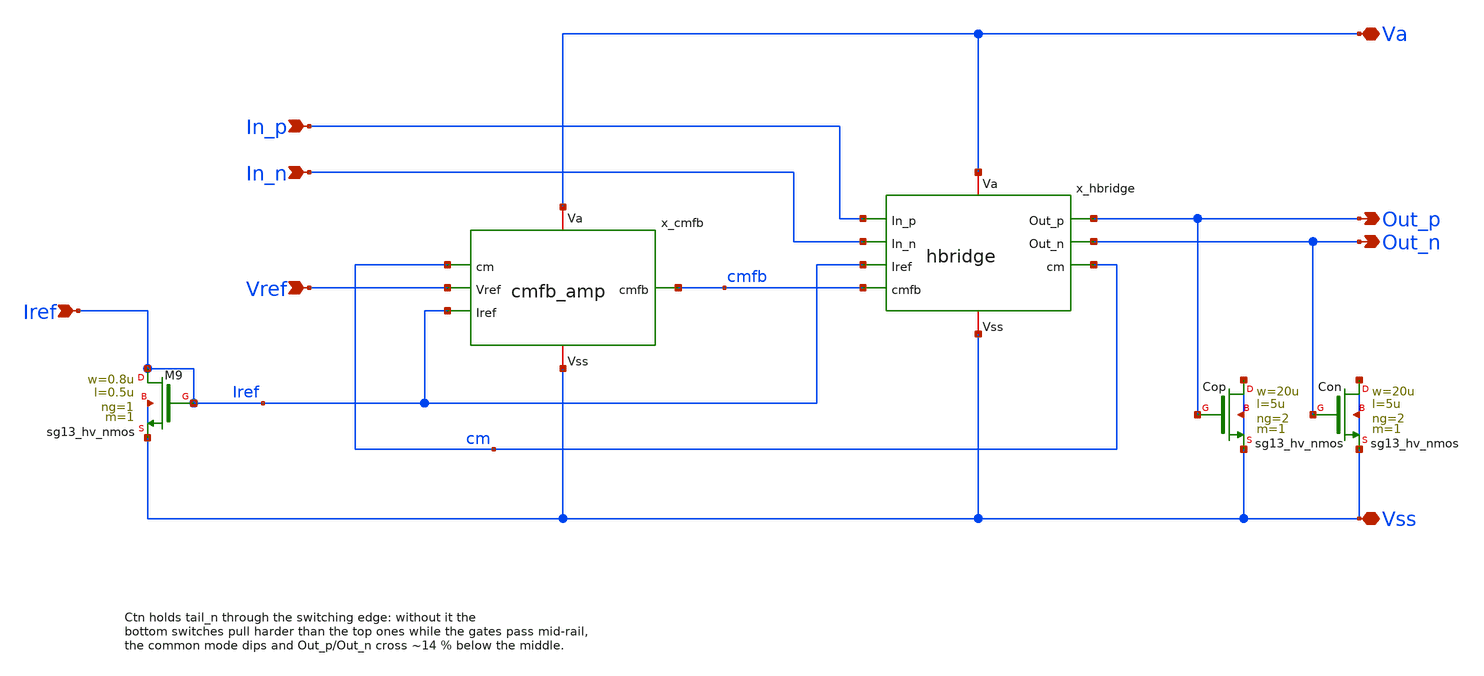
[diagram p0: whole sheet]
** sch_path: macros/lvds_tx/schematic/xschem/Driver.sch
**.subckt Driver Va Out_p Out_n Vref In_p In_n Vss Iref
*.iopin Va
*.opin Out_p
*.opin Out_n
*.ipin Vref
*.ipin In_p
*.ipin In_n
*.iopin Vss
*.ipin Iref
XM9 Iref Iref Vss Vss sg13_hv_nmos w=0.8u l=0.5u ng=1 m=1 mm_ok=1
XCop Vss Out_p Vss Vss sg13_hv_nmos w=20u l=5u ng=2 m=1 mm_ok=1
XCon Vss Out_n Vss Vss sg13_hv_nmos w=20u l=5u ng=2 m=1 mm_ok=1
x_cmfb cm Vref Iref cmfb Va Vss cmfb_amp
x_hbridge In_p In_n Iref cmfb Out_p Out_n cm Va Vss hbridge
**.ends

* expanding   symbol:  cmfb_amp.sym # of pins=6
** sym_path: macros/lvds_tx/schematic/xschem/cmfb_amp.sym
** sch_path: macros/lvds_tx/schematic/xschem/cmfb_amp.sch
.subckt cmfb_amp cm Vref Iref cmfb Va Vss
*.iopin Va
*.iopin Vss
*.ipin cm
*.ipin Iref
*.ipin Vref
*.opin cmfb
XM13 pd pd Va Va sg13_hv_pmos w=5u l=1u ng=1 m=1 mm_ok=1
XM14 cmfb pd Va Va sg13_hv_pmos w=5u l=1u ng=1 m=1 mm_ok=1
XM11 pd cm otail Vss sg13_hv_nmos w=20u l=1u ng=4 m=1 mm_ok=1
XM12 cmfb Vref otail Vss sg13_hv_nmos w=20u l=1u ng=4 m=1 mm_ok=1
XM10 otail Iref Vss Vss sg13_hv_nmos w=0.8u l=0.5u ng=1 m=1 mm_ok=1
XCc Vss cc_g Vss Vss sg13_hv_nmos w=50u l=5u ng=5 m=1 mm_ok=1
XRc cmfb cc_g Vss rppd w=1u l=6u m=1 b=0 mm_ok=1
.ends


* expanding   symbol:  hbridge.sym # of pins=9
** sym_path: macros/lvds_tx/schematic/xschem/hbridge.sym
** sch_path: macros/lvds_tx/schematic/xschem/hbridge.sch
.subckt hbridge In_p In_n Iref cmfb Out_p Out_n cm Va Vss
*.iopin Va
*.iopin Vss
*.ipin In_p
*.ipin In_n
*.ipin Iref
*.ipin cmfb
*.opin Out_p
*.opin Out_n
*.opin cm
XCtn Vss tail_n Vss Vss sg13_hv_nmos w=30u l=5u ng=3 m=1 mm_ok=1
XM2 tail_p cmfb Va Va sg13_hv_pmos w=97.2u l=0.5u ng=20 m=1 mm_ok=1
XM5 Out_p In_p tail_p Va sg13_hv_pmos w=80u l=0.4u ng=16 m=1 mm_ok=1
XM4 Out_n In_n tail_p Va sg13_hv_pmos w=80u l=0.4u ng=16 m=1 mm_ok=1
XM1 Out_p In_p tail_n Vss sg13_hv_nmos w=30u l=0.45u ng=15 m=1 mm_ok=1
XM3 Out_n In_n tail_n Vss sg13_hv_nmos w=30u l=0.45u ng=15 m=1 mm_ok=1
XM6 tail_n Iref Vss Vss sg13_hv_nmos w=99.2u l=0.5u ng=31 m=1 mm_ok=1
XRp Out_p cm Vss rhigh w=1u l=7.35u m=1 b=0 mm_ok=1
XRn Out_n cm Vss rhigh w=1u l=7.35u m=1 b=0 mm_ok=1
.ends

.end
